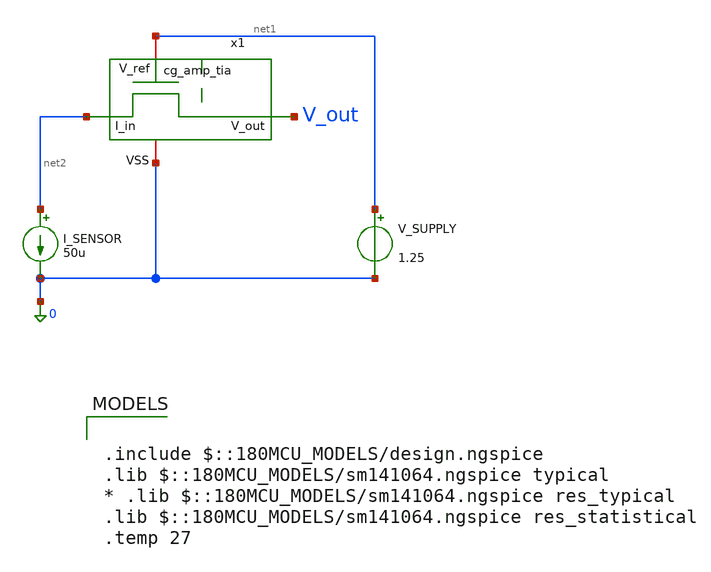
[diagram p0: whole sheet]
** sch_path: lvs/schematics/tb_cg_amp_tia.sch
**.subckt tb_cg_amp_tia
V_SUPPLY net1 0 1.25
I_SENSOR net2 0 50u
x1 net1 V_out net2 0 cg_amp_tia
**** begin user architecture code

.include $::180MCU_MODELS/design.ngspice
.lib $::180MCU_MODELS/sm141064.ngspice typical
* .lib $::180MCU_MODELS/sm141064.ngspice res_typical
.lib $::180MCU_MODELS/sm141064.ngspice res_statistical
.temp 27



.control
  op
  print v(V_out)
  print @m.x1.xm1.m0[vgs] @m.x1.xm1.m0[vth] @m.x1.xm1.m0[vdsat] @m.x1.xm1.m0[id] @m.x1.xm1.m0[gm]
+ @m.x1.xm1.m0[gds]
  print @r.x1.xr1.rt1[resistance] @r.x1.xr1.rt2[resistance]

  dc I_SENSOR 0 50u 1u
  let V_out_swp = v(V_out)
  plot V_out_swp title "CG-TIA: Sensor Current to Voltage"
  wrdata /foss/designs/analog-perceptron-gf180mcu/plots/cg_amp_tia_sweep.txt V_out_swp
  * === Op Sweep: M1 headroom across full 0-50uA input range ===
  save all @m.x1.xm1.m0[vgs] @m.x1.xm1.m0[vth] @m.x1.xm1.m0[vdsat] @m.x1.xm1.m0[id] @m.x1.xm1.m0[gm]
+ @m.x1.xm1.m0[gds]
  dc I_SENSOR 0 50u 1u
  wrdata /foss/designs/analog-perceptron-gf180mcu/plots/opsweep_cg_amp_tia.txt v(V_out)
+ @m.x1.xm1.m0[vgs] @m.x1.xm1.m0[vth] @m.x1.xm1.m0[vdsat] @m.x1.xm1.m0[id] @m.x1.xm1.m0[gm] @m.x1.xm1.m0[gds]
.endc


**** end user architecture code
**.ends

* expanding   symbol:  analog-perceptron-gf180mcu/lvs/schematics/cg_amp_tia.sym # of pins=4
** sym_path: schematics/cg_amp_tia.sym
** sch_path: schematics/cg_amp_tia.sch
.subckt cg_amp_tia V_ref V_out I_in VSS
*.iopin V_ref
*.iopin VSS
*.ipin I_in
*.opin V_out
XM1 V_out V_ref I_in VSS nfet_03v3 L=0.5u W=5u nf=1 ad='int((nf+1)/2) * W/nf * 0.18u' as='int((nf+2)/2) * W/nf * 0.18u'
+ pd='2*int((nf+1)/2) * (W/nf + 0.18u)' ps='2*int((nf+2)/2) * (W/nf + 0.18u)' nrd='0.18u / W' nrs='0.18u / W'
+ sa=0 sb=0 sd=0 m=1
XR1 V_out V_ref VSS ppolyf_u_1k r_width=3e-6 r_length=8.1e-6 m=1
.ends

.end
